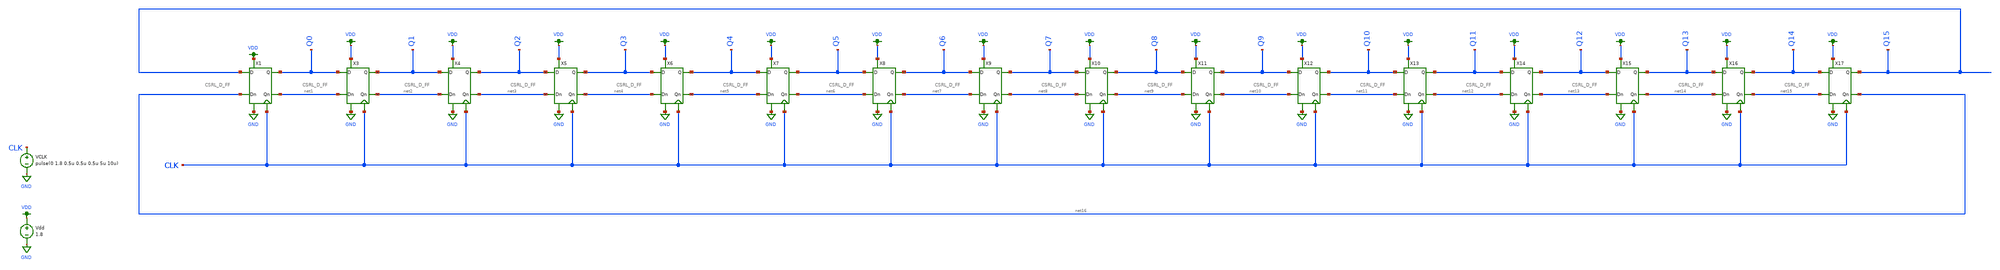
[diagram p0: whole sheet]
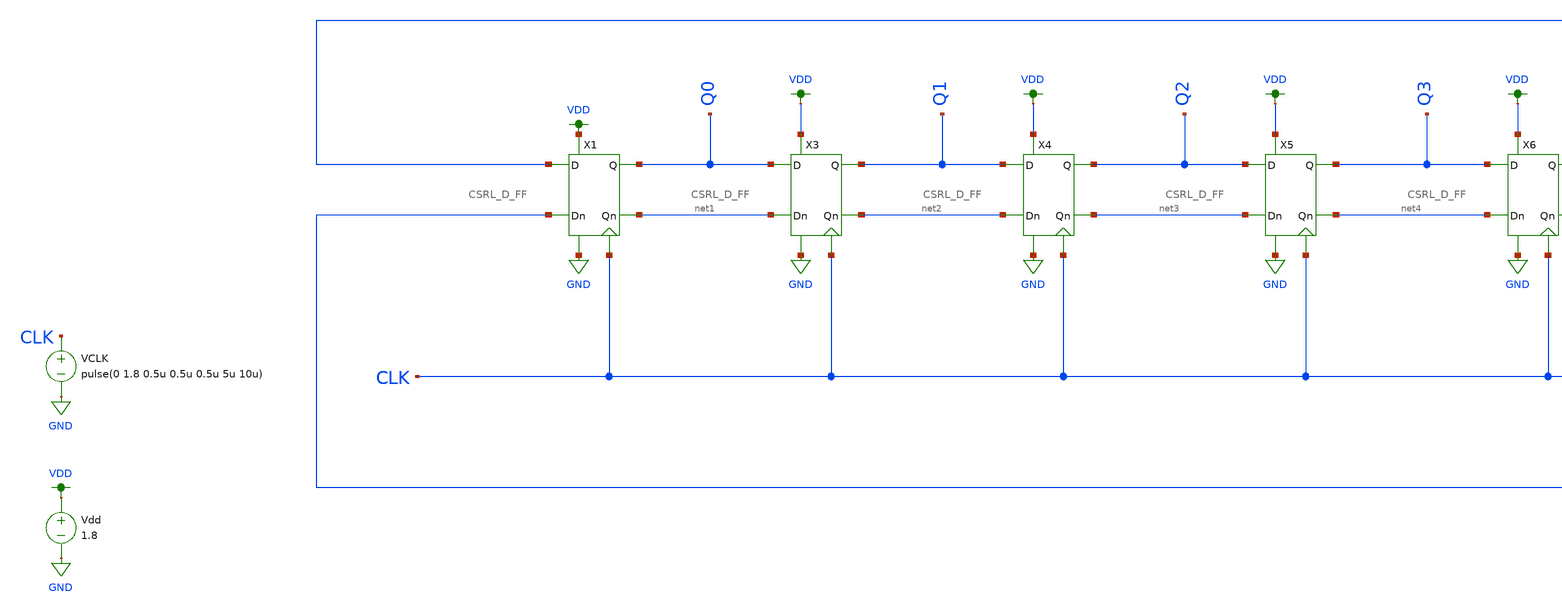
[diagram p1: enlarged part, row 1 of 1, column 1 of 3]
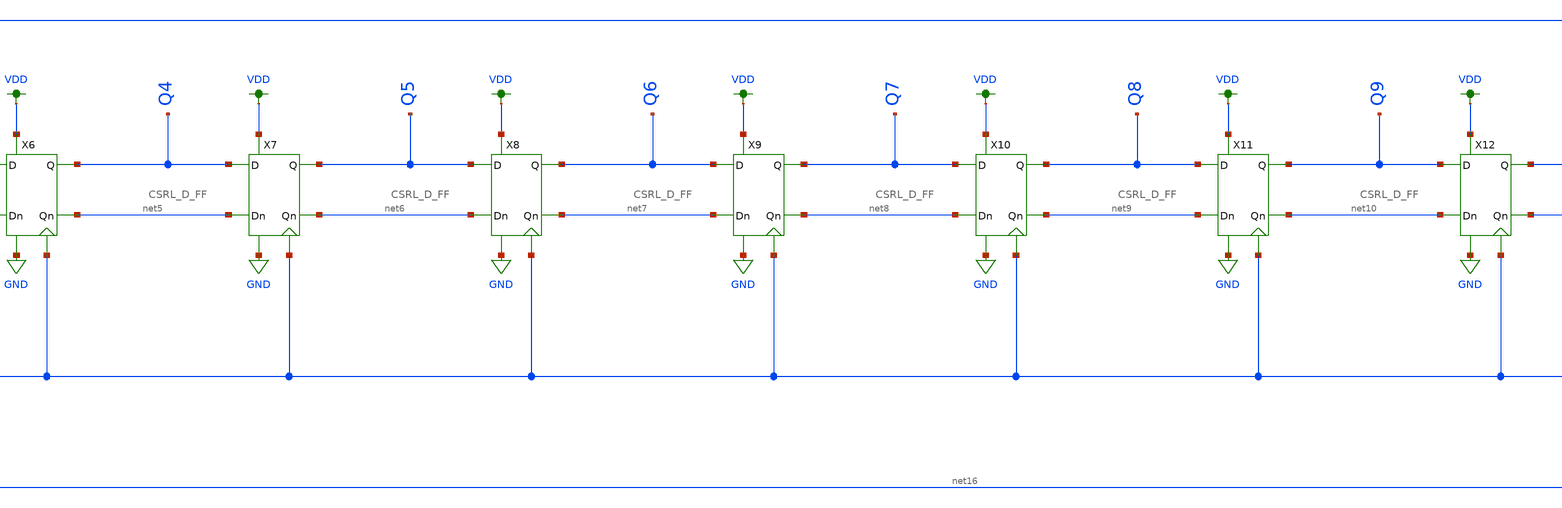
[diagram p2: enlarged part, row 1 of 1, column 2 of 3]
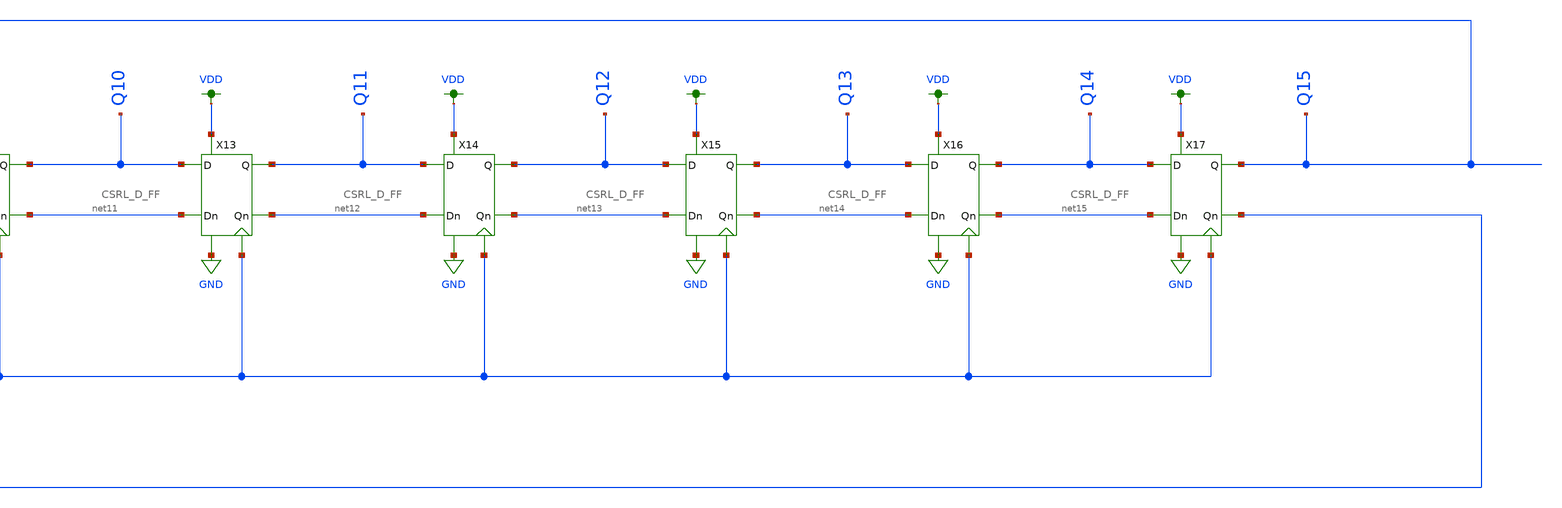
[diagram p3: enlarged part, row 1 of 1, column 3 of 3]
** sch_path: schematic/archive/phi1-new-circular.sch
**.subckt phi1-new-circular
VCLK CLK GND pulse(0 1.8 0.5u 0.5u 0.5u 5u 10u)
Vdd VDD GND 1.8
X3 net1 Q0 net2 Q1 GND VDD CLK CSRL_D_FF
X4 net2 Q1 net3 Q2 GND VDD CLK CSRL_D_FF
X5 net3 Q2 net4 Q3 GND VDD CLK CSRL_D_FF
X6 net4 Q3 net5 Q4 GND VDD CLK CSRL_D_FF
X7 net5 Q4 net6 Q5 GND VDD CLK CSRL_D_FF
X8 net6 Q5 net7 Q6 GND VDD CLK CSRL_D_FF
X9 net7 Q6 net8 Q7 GND VDD CLK CSRL_D_FF
X10 net8 Q7 net9 Q8 GND VDD CLK CSRL_D_FF
X11 net9 Q8 net10 Q9 GND VDD CLK CSRL_D_FF
X12 net10 Q9 net11 Q10 GND VDD CLK CSRL_D_FF
X13 net11 Q10 net12 Q11 GND VDD CLK CSRL_D_FF
X14 net12 Q11 net13 Q12 GND VDD CLK CSRL_D_FF
X15 net13 Q12 net14 Q13 GND VDD CLK CSRL_D_FF
X16 net14 Q13 net15 Q14 GND VDD CLK CSRL_D_FF
X17 net15 Q14 net16 Q15 GND VDD CLK CSRL_D_FF
X1 net16 Q15 net1 Q0 GND VDD CLK CSRL_D_FF
**** begin user architecture code

.ic v(Q0)=0 v(Q1)=0 v(Q2)=0 v(Q3)=0 v(Q4)=1 v(Q5)=1 v(Q6)=1 v(Q7)=1 v(Q8)=0 v(Q9)=0 v(Q10)=1
+ v(Q11)=1 v(Q12)=0 v(Q13)=0 v(Q14)=1 v(Q15)=1
.tran 0.5u 50u
.save all


.option wnflag=1
.param MC_SWITCH=0.0
.lib ~/skywater/skywater-pdk/libraries/sky130_fd_pr_ngspice/latest/models/sky130.lib.spice tt

**** end user architecture code
**.ends

* expanding   symbol:  /home/madvlsi/Documents/MADVLSI-Final_Project/schematic/CSRL_D_FF.sym # of
*+ pins=7
** sym_path: schematic/CSRL_D_FF.sym
** sch_path: schematic/CSRL_D_FF.sch
.subckt CSRL_D_FF Dn D Qn Q VN VP CLK
*.ipin Dn
*.ipin D
*.iopin VP
*.iopin VN
*.iopin CLK
*.opin Qn
*.opin Q
XM1 net5 CLK VP VDD sky130_fd_pr__pfet_01v8 L=0.15 W=1 nf=1 ad='int((nf+1)/2) * W/nf * 0.29' as='int((nf+2)/2) * W/nf * 0.29'
+ pd='2*int((nf+1)/2) * (W/nf + 0.29)' ps='2*int((nf+2)/2) * (W/nf + 0.29)' nrd='0.29 / W' nrs='0.29 / W'
+ sa=0 sb=0 sd=0 mult=1 m=1
XM2 net6 CLK VP VDD sky130_fd_pr__pfet_01v8 L=0.15 W=1 nf=1 ad='int((nf+1)/2) * W/nf * 0.29' as='int((nf+2)/2) * W/nf * 0.29'
+ pd='2*int((nf+1)/2) * (W/nf + 0.29)' ps='2*int((nf+2)/2) * (W/nf + 0.29)' nrd='0.29 / W' nrs='0.29 / W'
+ sa=0 sb=0 sd=0 mult=1 m=1
XM3 net3 CLK Q GND sky130_fd_pr__nfet_01v8 L=0.15 W=1 nf=1 ad='int((nf+1)/2) * W/nf * 0.29' as='int((nf+2)/2) * W/nf * 0.29'
+ pd='2*int((nf+1)/2) * (W/nf + 0.29)' ps='2*int((nf+2)/2) * (W/nf + 0.29)' nrd='0.29 / W' nrs='0.29 / W'
+ sa=0 sb=0 sd=0 mult=1 m=1
XM4 net4 CLK Qn GND sky130_fd_pr__nfet_01v8 L=0.15 W=1 nf=1 ad='int((nf+1)/2) * W/nf * 0.29' as='int((nf+2)/2) * W/nf * 0.29'
+ pd='2*int((nf+1)/2) * (W/nf + 0.29)' ps='2*int((nf+2)/2) * (W/nf + 0.29)' nrd='0.29 / W' nrs='0.29 / W'
+ sa=0 sb=0 sd=0 mult=1 m=1
XM5 Q Qn net6 VDD sky130_fd_pr__pfet_01v8 L=0.15 W=1 nf=1 ad='int((nf+1)/2) * W/nf * 0.29' as='int((nf+2)/2) * W/nf * 0.29'
+ pd='2*int((nf+1)/2) * (W/nf + 0.29)' ps='2*int((nf+2)/2) * (W/nf + 0.29)' nrd='0.29 / W' nrs='0.29 / W'
+ sa=0 sb=0 sd=0 mult=1 m=1
XM6 VN Qn Q GND sky130_fd_pr__nfet_01v8 L=0.15 W=1 nf=1 ad='int((nf+1)/2) * W/nf * 0.29' as='int((nf+2)/2) * W/nf * 0.29'
+ pd='2*int((nf+1)/2) * (W/nf + 0.29)' ps='2*int((nf+2)/2) * (W/nf + 0.29)' nrd='0.29 / W' nrs='0.29 / W'
+ sa=0 sb=0 sd=0 mult=1 m=1
XM7 Qn Q net5 VDD sky130_fd_pr__pfet_01v8 L=0.15 W=1 nf=1 ad='int((nf+1)/2) * W/nf * 0.29' as='int((nf+2)/2) * W/nf * 0.29'
+ pd='2*int((nf+1)/2) * (W/nf + 0.29)' ps='2*int((nf+2)/2) * (W/nf + 0.29)' nrd='0.29 / W' nrs='0.29 / W'
+ sa=0 sb=0 sd=0 mult=1 m=1
XM8 VN Q Qn GND sky130_fd_pr__nfet_01v8 L=0.15 W=1 nf=1 ad='int((nf+1)/2) * W/nf * 0.29' as='int((nf+2)/2) * W/nf * 0.29'
+ pd='2*int((nf+1)/2) * (W/nf + 0.29)' ps='2*int((nf+2)/2) * (W/nf + 0.29)' nrd='0.29 / W' nrs='0.29 / W'
+ sa=0 sb=0 sd=0 mult=1 m=1
XM9 net4 CLK Dn VDD sky130_fd_pr__pfet_01v8 L=0.15 W=1 nf=1 ad='int((nf+1)/2) * W/nf * 0.29' as='int((nf+2)/2) * W/nf * 0.29'
+ pd='2*int((nf+1)/2) * (W/nf + 0.29)' ps='2*int((nf+2)/2) * (W/nf + 0.29)' nrd='0.29 / W' nrs='0.29 / W'
+ sa=0 sb=0 sd=0 mult=1 m=1
XM10 net3 CLK D VDD sky130_fd_pr__pfet_01v8 L=0.15 W=1 nf=1 ad='int((nf+1)/2) * W/nf * 0.29' as='int((nf+2)/2) * W/nf * 0.29'
+ pd='2*int((nf+1)/2) * (W/nf + 0.29)' ps='2*int((nf+2)/2) * (W/nf + 0.29)' nrd='0.29 / W' nrs='0.29 / W'
+ sa=0 sb=0 sd=0 mult=1 m=1
XM11 VN CLK net1 GND sky130_fd_pr__nfet_01v8 L=0.15 W=1 nf=1 ad='int((nf+1)/2) * W/nf * 0.29' as='int((nf+2)/2) * W/nf * 0.29'
+ pd='2*int((nf+1)/2) * (W/nf + 0.29)' ps='2*int((nf+2)/2) * (W/nf + 0.29)' nrd='0.29 / W' nrs='0.29 / W'
+ sa=0 sb=0 sd=0 mult=1 m=1
XM12 VN CLK net2 GND sky130_fd_pr__nfet_01v8 L=0.15 W=1 nf=1 ad='int((nf+1)/2) * W/nf * 0.29' as='int((nf+2)/2) * W/nf * 0.29'
+ pd='2*int((nf+1)/2) * (W/nf + 0.29)' ps='2*int((nf+2)/2) * (W/nf + 0.29)' nrd='0.29 / W' nrs='0.29 / W'
+ sa=0 sb=0 sd=0 mult=1 m=1
XM13 VP net3 net4 VDD sky130_fd_pr__pfet_01v8 L=0.15 W=1 nf=1 ad='int((nf+1)/2) * W/nf * 0.29' as='int((nf+2)/2) * W/nf * 0.29'
+ pd='2*int((nf+1)/2) * (W/nf + 0.29)' ps='2*int((nf+2)/2) * (W/nf + 0.29)' nrd='0.29 / W' nrs='0.29 / W'
+ sa=0 sb=0 sd=0 mult=1 m=1
XM14 VP net4 net3 VDD sky130_fd_pr__pfet_01v8 L=0.15 W=1 nf=1 ad='int((nf+1)/2) * W/nf * 0.29' as='int((nf+2)/2) * W/nf * 0.29'
+ pd='2*int((nf+1)/2) * (W/nf + 0.29)' ps='2*int((nf+2)/2) * (W/nf + 0.29)' nrd='0.29 / W' nrs='0.29 / W'
+ sa=0 sb=0 sd=0 mult=1 m=1
XM15 net3 net4 net1 GND sky130_fd_pr__nfet_01v8 L=0.15 W=1 nf=1 ad='int((nf+1)/2) * W/nf * 0.29' as='int((nf+2)/2) * W/nf * 0.29'
+ pd='2*int((nf+1)/2) * (W/nf + 0.29)' ps='2*int((nf+2)/2) * (W/nf + 0.29)' nrd='0.29 / W' nrs='0.29 / W'
+ sa=0 sb=0 sd=0 mult=1 m=1
XM16 net4 net3 net2 GND sky130_fd_pr__nfet_01v8 L=0.15 W=1 nf=1 ad='int((nf+1)/2) * W/nf * 0.29' as='int((nf+2)/2) * W/nf * 0.29'
+ pd='2*int((nf+1)/2) * (W/nf + 0.29)' ps='2*int((nf+2)/2) * (W/nf + 0.29)' nrd='0.29 / W' nrs='0.29 / W'
+ sa=0 sb=0 sd=0 mult=1 m=1
XM17 VN CLK net2 GND sky130_fd_pr__nfet_01v8 L=0.15 W=1 nf=1 ad='int((nf+1)/2) * W/nf * 0.29' as='int((nf+2)/2) * W/nf * 0.29'
+ pd='2*int((nf+1)/2) * (W/nf + 0.29)' ps='2*int((nf+2)/2) * (W/nf + 0.29)' nrd='0.29 / W' nrs='0.29 / W'
+ sa=0 sb=0 sd=0 mult=1 m=1
XM18 VN CLK net1 GND sky130_fd_pr__nfet_01v8 L=0.15 W=1 nf=1 ad='int((nf+1)/2) * W/nf * 0.29' as='int((nf+2)/2) * W/nf * 0.29'
+ pd='2*int((nf+1)/2) * (W/nf + 0.29)' ps='2*int((nf+2)/2) * (W/nf + 0.29)' nrd='0.29 / W' nrs='0.29 / W'
+ sa=0 sb=0 sd=0 mult=1 m=1
.ends

.GLOBAL GND
.GLOBAL VDD
.end
